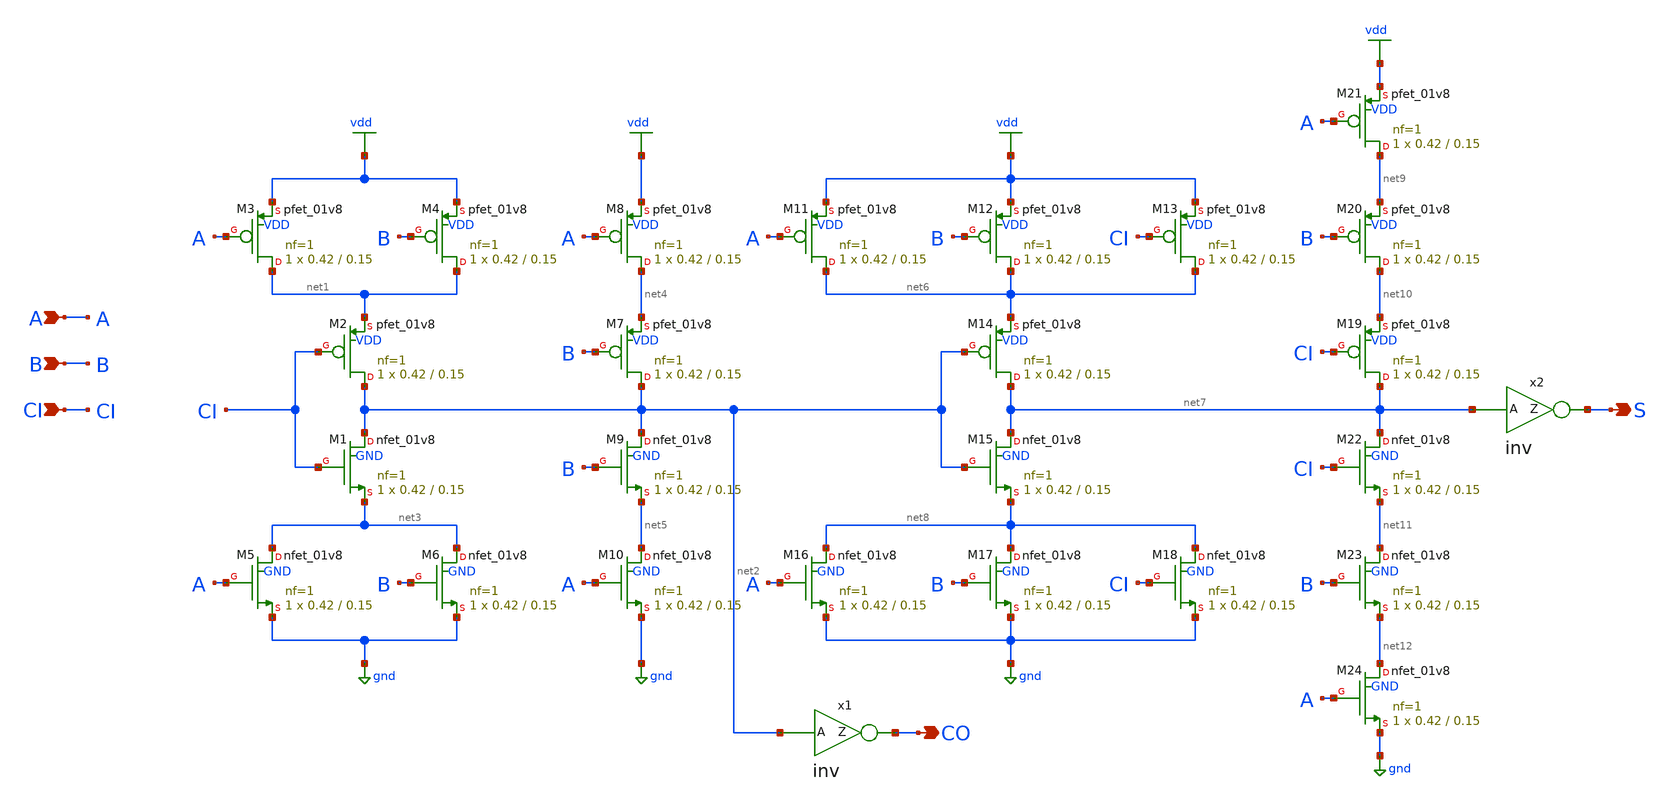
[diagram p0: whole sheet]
** sch_path: xschem/addf.sch
**.subckt addf A B CI S CO
*.ipin A
*.ipin B
*.ipin CI
*.opin S
*.opin CO
XM1 net2 CI net3 GND sky130_fd_pr__nfet_01v8 L=0.15 W=0.42 nf=1 ad='int((nf+1)/2) * W/nf * 0.29' as='int((nf+2)/2) * W/nf * 0.29'
+ pd='2*int((nf+1)/2) * (W/nf + 0.29)' ps='2*int((nf+2)/2) * (W/nf + 0.29)' nrd='0.29 / W' nrs='0.29 / W'
+ sa=0 sb=0 sd=0 mult=1 m=1
XM2 net2 CI net1 VDD sky130_fd_pr__pfet_01v8 L=0.15 W=0.42 nf=1 ad='int((nf+1)/2) * W/nf * 0.29' as='int((nf+2)/2) * W/nf * 0.29'
+ pd='2*int((nf+1)/2) * (W/nf + 0.29)' ps='2*int((nf+2)/2) * (W/nf + 0.29)' nrd='0.29 / W' nrs='0.29 / W'
+ sa=0 sb=0 sd=0 mult=1 m=1
XM3 net1 A vdd VDD sky130_fd_pr__pfet_01v8 L=0.15 W=0.42 nf=1 ad='int((nf+1)/2) * W/nf * 0.29' as='int((nf+2)/2) * W/nf * 0.29'
+ pd='2*int((nf+1)/2) * (W/nf + 0.29)' ps='2*int((nf+2)/2) * (W/nf + 0.29)' nrd='0.29 / W' nrs='0.29 / W'
+ sa=0 sb=0 sd=0 mult=1 m=1
XM4 net1 B vdd VDD sky130_fd_pr__pfet_01v8 L=0.15 W=0.42 nf=1 ad='int((nf+1)/2) * W/nf * 0.29' as='int((nf+2)/2) * W/nf * 0.29'
+ pd='2*int((nf+1)/2) * (W/nf + 0.29)' ps='2*int((nf+2)/2) * (W/nf + 0.29)' nrd='0.29 / W' nrs='0.29 / W'
+ sa=0 sb=0 sd=0 mult=1 m=1
XM5 net3 A gnd GND sky130_fd_pr__nfet_01v8 L=0.15 W=0.42 nf=1 ad='int((nf+1)/2) * W/nf * 0.29' as='int((nf+2)/2) * W/nf * 0.29'
+ pd='2*int((nf+1)/2) * (W/nf + 0.29)' ps='2*int((nf+2)/2) * (W/nf + 0.29)' nrd='0.29 / W' nrs='0.29 / W'
+ sa=0 sb=0 sd=0 mult=1 m=1
XM6 net3 B gnd GND sky130_fd_pr__nfet_01v8 L=0.15 W=0.42 nf=1 ad='int((nf+1)/2) * W/nf * 0.29' as='int((nf+2)/2) * W/nf * 0.29'
+ pd='2*int((nf+1)/2) * (W/nf + 0.29)' ps='2*int((nf+2)/2) * (W/nf + 0.29)' nrd='0.29 / W' nrs='0.29 / W'
+ sa=0 sb=0 sd=0 mult=1 m=1
XM7 net2 B net4 VDD sky130_fd_pr__pfet_01v8 L=0.15 W=0.42 nf=1 ad='int((nf+1)/2) * W/nf * 0.29' as='int((nf+2)/2) * W/nf * 0.29'
+ pd='2*int((nf+1)/2) * (W/nf + 0.29)' ps='2*int((nf+2)/2) * (W/nf + 0.29)' nrd='0.29 / W' nrs='0.29 / W'
+ sa=0 sb=0 sd=0 mult=1 m=1
XM8 net4 A vdd VDD sky130_fd_pr__pfet_01v8 L=0.15 W=0.42 nf=1 ad='int((nf+1)/2) * W/nf * 0.29' as='int((nf+2)/2) * W/nf * 0.29'
+ pd='2*int((nf+1)/2) * (W/nf + 0.29)' ps='2*int((nf+2)/2) * (W/nf + 0.29)' nrd='0.29 / W' nrs='0.29 / W'
+ sa=0 sb=0 sd=0 mult=1 m=1
XM9 net2 B net5 GND sky130_fd_pr__nfet_01v8 L=0.15 W=0.42 nf=1 ad='int((nf+1)/2) * W/nf * 0.29' as='int((nf+2)/2) * W/nf * 0.29'
+ pd='2*int((nf+1)/2) * (W/nf + 0.29)' ps='2*int((nf+2)/2) * (W/nf + 0.29)' nrd='0.29 / W' nrs='0.29 / W'
+ sa=0 sb=0 sd=0 mult=1 m=1
XM10 net5 A gnd GND sky130_fd_pr__nfet_01v8 L=0.15 W=0.42 nf=1 ad='int((nf+1)/2) * W/nf * 0.29' as='int((nf+2)/2) * W/nf * 0.29'
+ pd='2*int((nf+1)/2) * (W/nf + 0.29)' ps='2*int((nf+2)/2) * (W/nf + 0.29)' nrd='0.29 / W' nrs='0.29 / W'
+ sa=0 sb=0 sd=0 mult=1 m=1
XM11 net6 A vdd VDD sky130_fd_pr__pfet_01v8 L=0.15 W=0.42 nf=1 ad='int((nf+1)/2) * W/nf * 0.29' as='int((nf+2)/2) * W/nf * 0.29'
+ pd='2*int((nf+1)/2) * (W/nf + 0.29)' ps='2*int((nf+2)/2) * (W/nf + 0.29)' nrd='0.29 / W' nrs='0.29 / W'
+ sa=0 sb=0 sd=0 mult=1 m=1
XM12 net6 B vdd VDD sky130_fd_pr__pfet_01v8 L=0.15 W=0.42 nf=1 ad='int((nf+1)/2) * W/nf * 0.29' as='int((nf+2)/2) * W/nf * 0.29'
+ pd='2*int((nf+1)/2) * (W/nf + 0.29)' ps='2*int((nf+2)/2) * (W/nf + 0.29)' nrd='0.29 / W' nrs='0.29 / W'
+ sa=0 sb=0 sd=0 mult=1 m=1
XM13 net6 CI vdd VDD sky130_fd_pr__pfet_01v8 L=0.15 W=0.42 nf=1 ad='int((nf+1)/2) * W/nf * 0.29' as='int((nf+2)/2) * W/nf * 0.29'
+ pd='2*int((nf+1)/2) * (W/nf + 0.29)' ps='2*int((nf+2)/2) * (W/nf + 0.29)' nrd='0.29 / W' nrs='0.29 / W'
+ sa=0 sb=0 sd=0 mult=1 m=1
XM14 net7 net2 net6 VDD sky130_fd_pr__pfet_01v8 L=0.15 W=0.42 nf=1 ad='int((nf+1)/2) * W/nf * 0.29' as='int((nf+2)/2) * W/nf * 0.29'
+ pd='2*int((nf+1)/2) * (W/nf + 0.29)' ps='2*int((nf+2)/2) * (W/nf + 0.29)' nrd='0.29 / W' nrs='0.29 / W'
+ sa=0 sb=0 sd=0 mult=1 m=1
XM15 net7 net2 net8 GND sky130_fd_pr__nfet_01v8 L=0.15 W=0.42 nf=1 ad='int((nf+1)/2) * W/nf * 0.29' as='int((nf+2)/2) * W/nf * 0.29'
+ pd='2*int((nf+1)/2) * (W/nf + 0.29)' ps='2*int((nf+2)/2) * (W/nf + 0.29)' nrd='0.29 / W' nrs='0.29 / W'
+ sa=0 sb=0 sd=0 mult=1 m=1
XM16 net8 A gnd GND sky130_fd_pr__nfet_01v8 L=0.15 W=0.42 nf=1 ad='int((nf+1)/2) * W/nf * 0.29' as='int((nf+2)/2) * W/nf * 0.29'
+ pd='2*int((nf+1)/2) * (W/nf + 0.29)' ps='2*int((nf+2)/2) * (W/nf + 0.29)' nrd='0.29 / W' nrs='0.29 / W'
+ sa=0 sb=0 sd=0 mult=1 m=1
XM17 net8 B gnd GND sky130_fd_pr__nfet_01v8 L=0.15 W=0.42 nf=1 ad='int((nf+1)/2) * W/nf * 0.29' as='int((nf+2)/2) * W/nf * 0.29'
+ pd='2*int((nf+1)/2) * (W/nf + 0.29)' ps='2*int((nf+2)/2) * (W/nf + 0.29)' nrd='0.29 / W' nrs='0.29 / W'
+ sa=0 sb=0 sd=0 mult=1 m=1
XM18 net8 CI gnd GND sky130_fd_pr__nfet_01v8 L=0.15 W=0.42 nf=1 ad='int((nf+1)/2) * W/nf * 0.29' as='int((nf+2)/2) * W/nf * 0.29'
+ pd='2*int((nf+1)/2) * (W/nf + 0.29)' ps='2*int((nf+2)/2) * (W/nf + 0.29)' nrd='0.29 / W' nrs='0.29 / W'
+ sa=0 sb=0 sd=0 mult=1 m=1
XM19 net7 CI net10 VDD sky130_fd_pr__pfet_01v8 L=0.15 W=0.42 nf=1 ad='int((nf+1)/2) * W/nf * 0.29' as='int((nf+2)/2) * W/nf * 0.29'
+ pd='2*int((nf+1)/2) * (W/nf + 0.29)' ps='2*int((nf+2)/2) * (W/nf + 0.29)' nrd='0.29 / W' nrs='0.29 / W'
+ sa=0 sb=0 sd=0 mult=1 m=1
XM20 net10 B net9 VDD sky130_fd_pr__pfet_01v8 L=0.15 W=0.42 nf=1 ad='int((nf+1)/2) * W/nf * 0.29' as='int((nf+2)/2) * W/nf * 0.29'
+ pd='2*int((nf+1)/2) * (W/nf + 0.29)' ps='2*int((nf+2)/2) * (W/nf + 0.29)' nrd='0.29 / W' nrs='0.29 / W'
+ sa=0 sb=0 sd=0 mult=1 m=1
XM21 net9 A vdd VDD sky130_fd_pr__pfet_01v8 L=0.15 W=0.42 nf=1 ad='int((nf+1)/2) * W/nf * 0.29' as='int((nf+2)/2) * W/nf * 0.29'
+ pd='2*int((nf+1)/2) * (W/nf + 0.29)' ps='2*int((nf+2)/2) * (W/nf + 0.29)' nrd='0.29 / W' nrs='0.29 / W'
+ sa=0 sb=0 sd=0 mult=1 m=1
XM22 net7 CI net11 GND sky130_fd_pr__nfet_01v8 L=0.15 W=0.42 nf=1 ad='int((nf+1)/2) * W/nf * 0.29' as='int((nf+2)/2) * W/nf * 0.29'
+ pd='2*int((nf+1)/2) * (W/nf + 0.29)' ps='2*int((nf+2)/2) * (W/nf + 0.29)' nrd='0.29 / W' nrs='0.29 / W'
+ sa=0 sb=0 sd=0 mult=1 m=1
XM23 net11 B net12 GND sky130_fd_pr__nfet_01v8 L=0.15 W=0.42 nf=1 ad='int((nf+1)/2) * W/nf * 0.29' as='int((nf+2)/2) * W/nf * 0.29'
+ pd='2*int((nf+1)/2) * (W/nf + 0.29)' ps='2*int((nf+2)/2) * (W/nf + 0.29)' nrd='0.29 / W' nrs='0.29 / W'
+ sa=0 sb=0 sd=0 mult=1 m=1
XM24 net12 A gnd GND sky130_fd_pr__nfet_01v8 L=0.15 W=0.42 nf=1 ad='int((nf+1)/2) * W/nf * 0.29' as='int((nf+2)/2) * W/nf * 0.29'
+ pd='2*int((nf+1)/2) * (W/nf + 0.29)' ps='2*int((nf+2)/2) * (W/nf + 0.29)' nrd='0.29 / W' nrs='0.29 / W'
+ sa=0 sb=0 sd=0 mult=1 m=1
x1 CO net2 inv
x2 S net7 inv
**.ends

* expanding   symbol:  inv.sym # of pins=2
** sym_path: xschem/inv.sym
** sch_path: xschem/inv.sch
.subckt inv Z A
*.ipin A
*.opin Z
XM1 Z A gnd GND sky130_fd_pr__nfet_01v8 L=0.15 W=0.42 nf=1 ad='int((nf+1)/2) * W/nf * 0.29' as='int((nf+2)/2) * W/nf * 0.29'
+ pd='2*int((nf+1)/2) * (W/nf + 0.29)' ps='2*int((nf+2)/2) * (W/nf + 0.29)' nrd='0.29 / W' nrs='0.29 / W'
+ sa=0 sb=0 sd=0 mult=1 m=1
XM2 Z A vdd VDD sky130_fd_pr__pfet_01v8 L=0.15 W=0.84 nf=1 ad='int((nf+1)/2) * W/nf * 0.29' as='int((nf+2)/2) * W/nf * 0.29'
+ pd='2*int((nf+1)/2) * (W/nf + 0.29)' ps='2*int((nf+2)/2) * (W/nf + 0.29)' nrd='0.29 / W' nrs='0.29 / W'
+ sa=0 sb=0 sd=0 mult=1 m=1
.ends

.GLOBAL vdd
.GLOBAL gnd
.end
